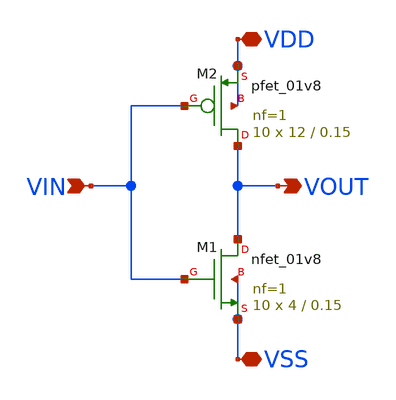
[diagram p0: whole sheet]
** sch_path: xschem/DC_DC_Converter_xschem/OTHERS/DC_DC_Converter_6/Inverter_2/Inverter2.sch
**.subckt Inverter2 VIN VDD VSS VOUT
*.ipin VIN
*.iopin VDD
*.iopin VSS
*.opin VOUT
XM1 VOUT VIN VSS VSS sky130_fd_pr__nfet_01v8 L=0.15 W=4 nf=1 ad='int((nf+1)/2) * W/nf * 0.29' as='int((nf+2)/2) * W/nf * 0.29'
+ pd='2*int((nf+1)/2) * (W/nf + 0.29)' ps='2*int((nf+2)/2) * (W/nf + 0.29)' nrd='0.29 / W' nrs='0.29 / W'
+ sa=0 sb=0 sd=0 mult=10 m=10
XM2 VOUT VIN VDD VDD sky130_fd_pr__pfet_01v8 L=0.15 W=12 nf=1 ad='int((nf+1)/2) * W/nf * 0.29' as='int((nf+2)/2) * W/nf * 0.29'
+ pd='2*int((nf+1)/2) * (W/nf + 0.29)' ps='2*int((nf+2)/2) * (W/nf + 0.29)' nrd='0.29 / W' nrs='0.29 / W'
+ sa=0 sb=0 sd=0 mult=10 m=10
**.ends
.end
